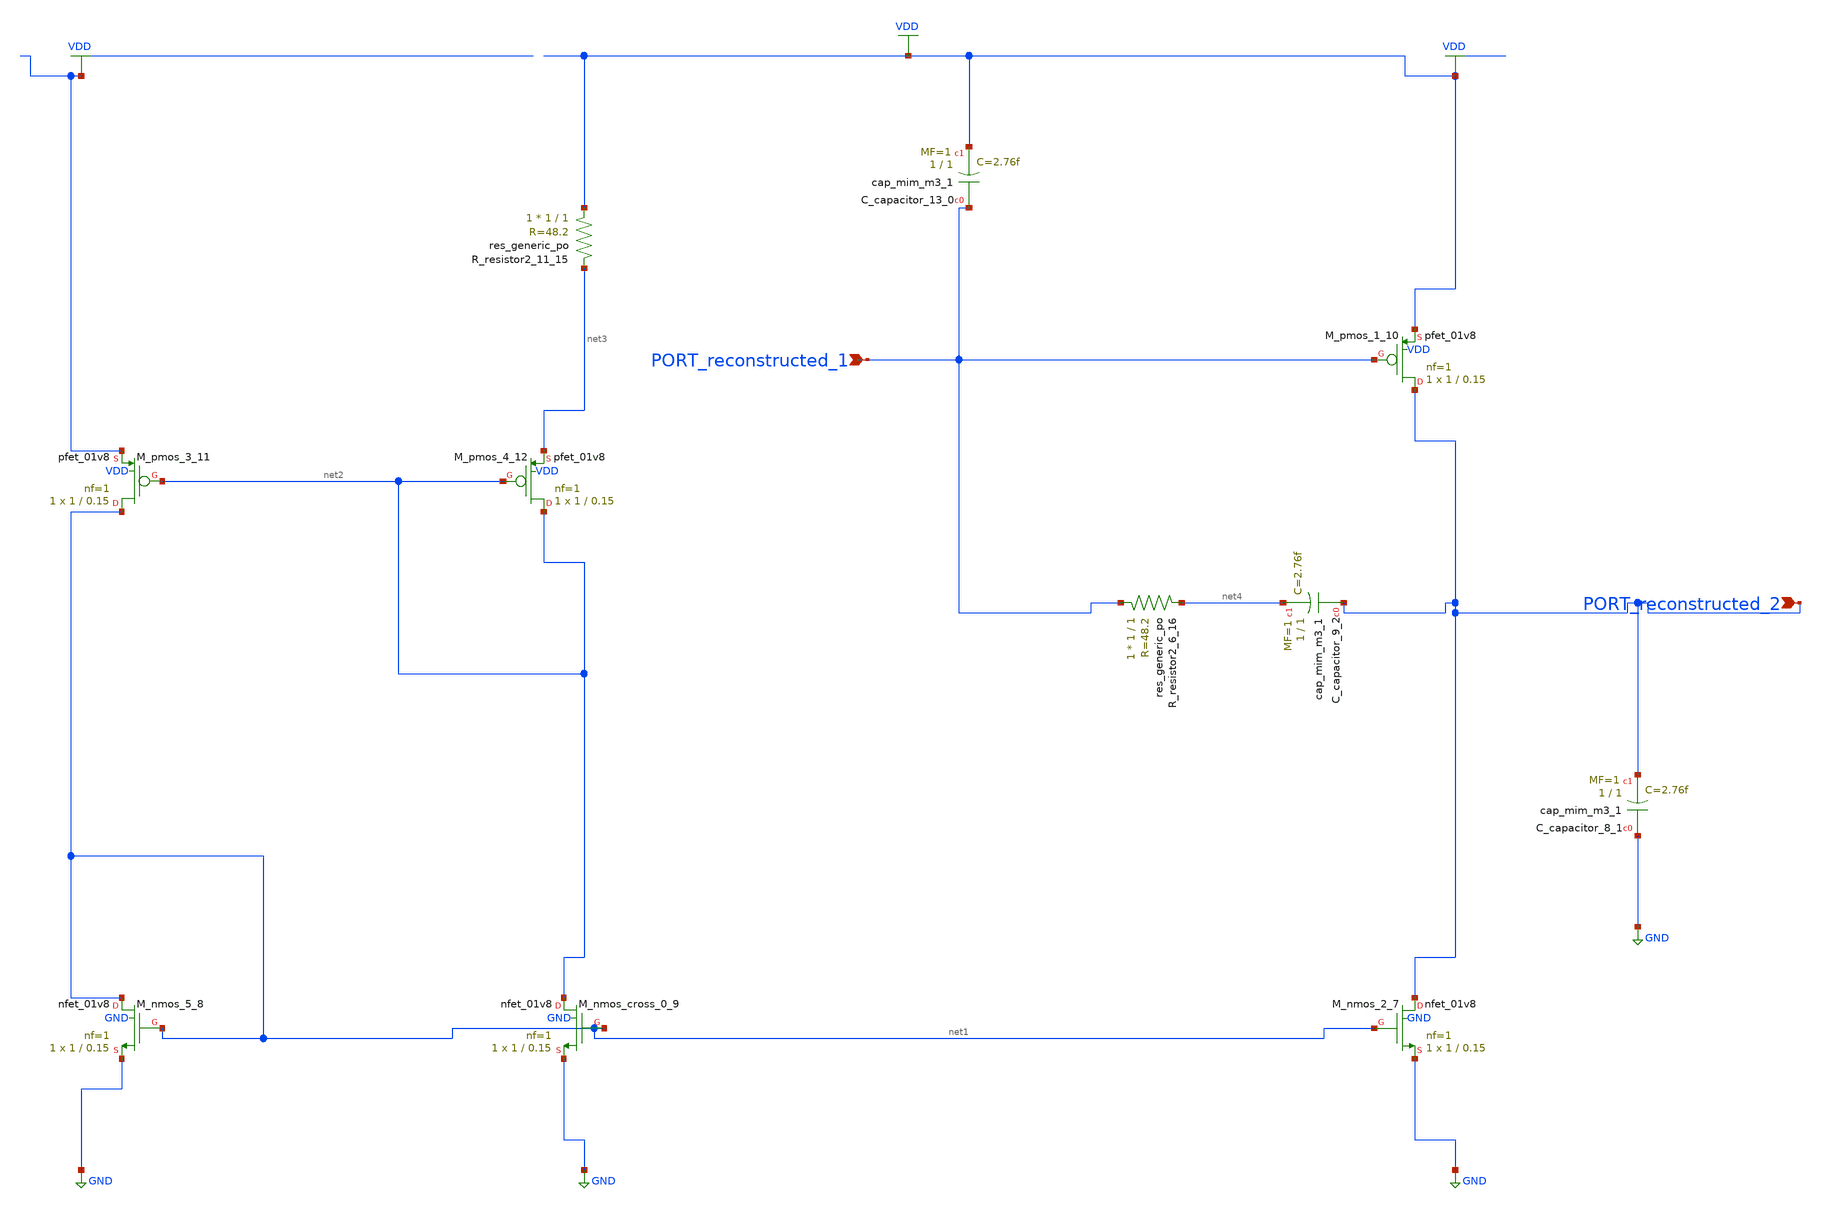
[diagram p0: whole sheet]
** sch_path: schematics/AMSNet/727.sch
**.subckt 727 PORT_reconstructed_2 PORT_reconstructed_1
*.ipin PORT_reconstructed_2
*.ipin PORT_reconstructed_1
XC_capacitor_13_0 PORT_reconstructed_1 VDD sky130_fd_pr__cap_mim_m3_1 W=1 L=1 MF=1 m=1
XC_capacitor_8_1 GND PORT_reconstructed_2 sky130_fd_pr__cap_mim_m3_1 W=1 L=1 MF=1 m=1
XC_capacitor_9_2 PORT_reconstructed_2 net4 sky130_fd_pr__cap_mim_m3_1 W=1 L=1 MF=1 m=1
XM_nmos_2_7 PORT_reconstructed_2 net1 GND GND sky130_fd_pr__nfet_01v8 L=0.15 W=1 nf=1 ad='int((1 + 1)/2) * 1 / 1 * 0.29'
+ as='int((1 + 2)/2) * 1 / 1 * 0.29' pd='2*int((1 + 1)/2) * (1 / 1 + 0.29)' ps='2*int((1 + 2)/2) * (1 / 1 + 0.29)'
+ nrd='0.29 / 1 ' nrs='0.29 / 1 ' sa=0 sb=0 sd=0 mult=1 m=1
XM_nmos_5_8 net1 net1 GND GND sky130_fd_pr__nfet_01v8 L=0.15 W=1 nf=1 ad='int((1 + 1)/2) * 1 / 1 * 0.29'
+ as='int((1 + 2)/2) * 1 / 1 * 0.29' pd='2*int((1 + 1)/2) * (1 / 1 + 0.29)' ps='2*int((1 + 2)/2) * (1 / 1 + 0.29)'
+ nrd='0.29 / 1 ' nrs='0.29 / 1 ' sa=0 sb=0 sd=0 mult=1 m=1
XM_nmos_cross_0_9 net2 net1 GND GND sky130_fd_pr__nfet_01v8 L=0.15 W=1 nf=1 ad='int((1 + 1)/2) * 1 / 1 * 0.29'
+ as='int((1 + 2)/2) * 1 / 1 * 0.29' pd='2*int((1 + 1)/2) * (1 / 1 + 0.29)' ps='2*int((1 + 2)/2) * (1 / 1 + 0.29)'
+ nrd='0.29 / 1 ' nrs='0.29 / 1 ' sa=0 sb=0 sd=0 mult=1 m=1
XM_pmos_1_10 PORT_reconstructed_2 PORT_reconstructed_1 VDD VDD sky130_fd_pr__pfet_01v8 L=0.15 W=1 nf=1
+ ad='int((1 + 1)/2) * 1 / 1 * 0.29' as='int((1 + 2)/2) * 1 / 1 * 0.29' pd='2*int((1 + 1)/2) * (1 / 1 + 0.29)'
+ ps='2*int((1 + 2)/2) * (1 / 1 + 0.29)' nrd='0.29 / 1 ' nrs='0.29 / 1 ' sa=0 sb=0 sd=0 mult=1 m=1
XM_pmos_3_11 net1 net2 VDD VDD sky130_fd_pr__pfet_01v8 L=0.15 W=1 nf=1 ad='int((1 + 1)/2) * 1 / 1 * 0.29'
+ as='int((1 + 2)/2) * 1 / 1 * 0.29' pd='2*int((1 + 1)/2) * (1 / 1 + 0.29)' ps='2*int((1 + 2)/2) * (1 / 1 + 0.29)'
+ nrd='0.29 / 1 ' nrs='0.29 / 1 ' sa=0 sb=0 sd=0 mult=1 m=1
XM_pmos_4_12 net2 net2 net3 VDD sky130_fd_pr__pfet_01v8 L=0.15 W=1 nf=1 ad='int((1 + 1)/2) * 1 / 1 * 0.29'
+ as='int((1 + 2)/2) * 1 / 1 * 0.29' pd='2*int((1 + 1)/2) * (1 / 1 + 0.29)' ps='2*int((1 + 2)/2) * (1 / 1 + 0.29)'
+ nrd='0.29 / 1 ' nrs='0.29 / 1 ' sa=0 sb=0 sd=0 mult=1 m=1
XR_resistor2_11_15 VDD net3 sky130_fd_pr__res_generic_po W=1 L=1 m=1
XR_resistor2_6_16 PORT_reconstructed_1 net4 sky130_fd_pr__res_generic_po W=1 L=1 m=1
**.ends
.GLOBAL GND
.GLOBAL VDD
.end
